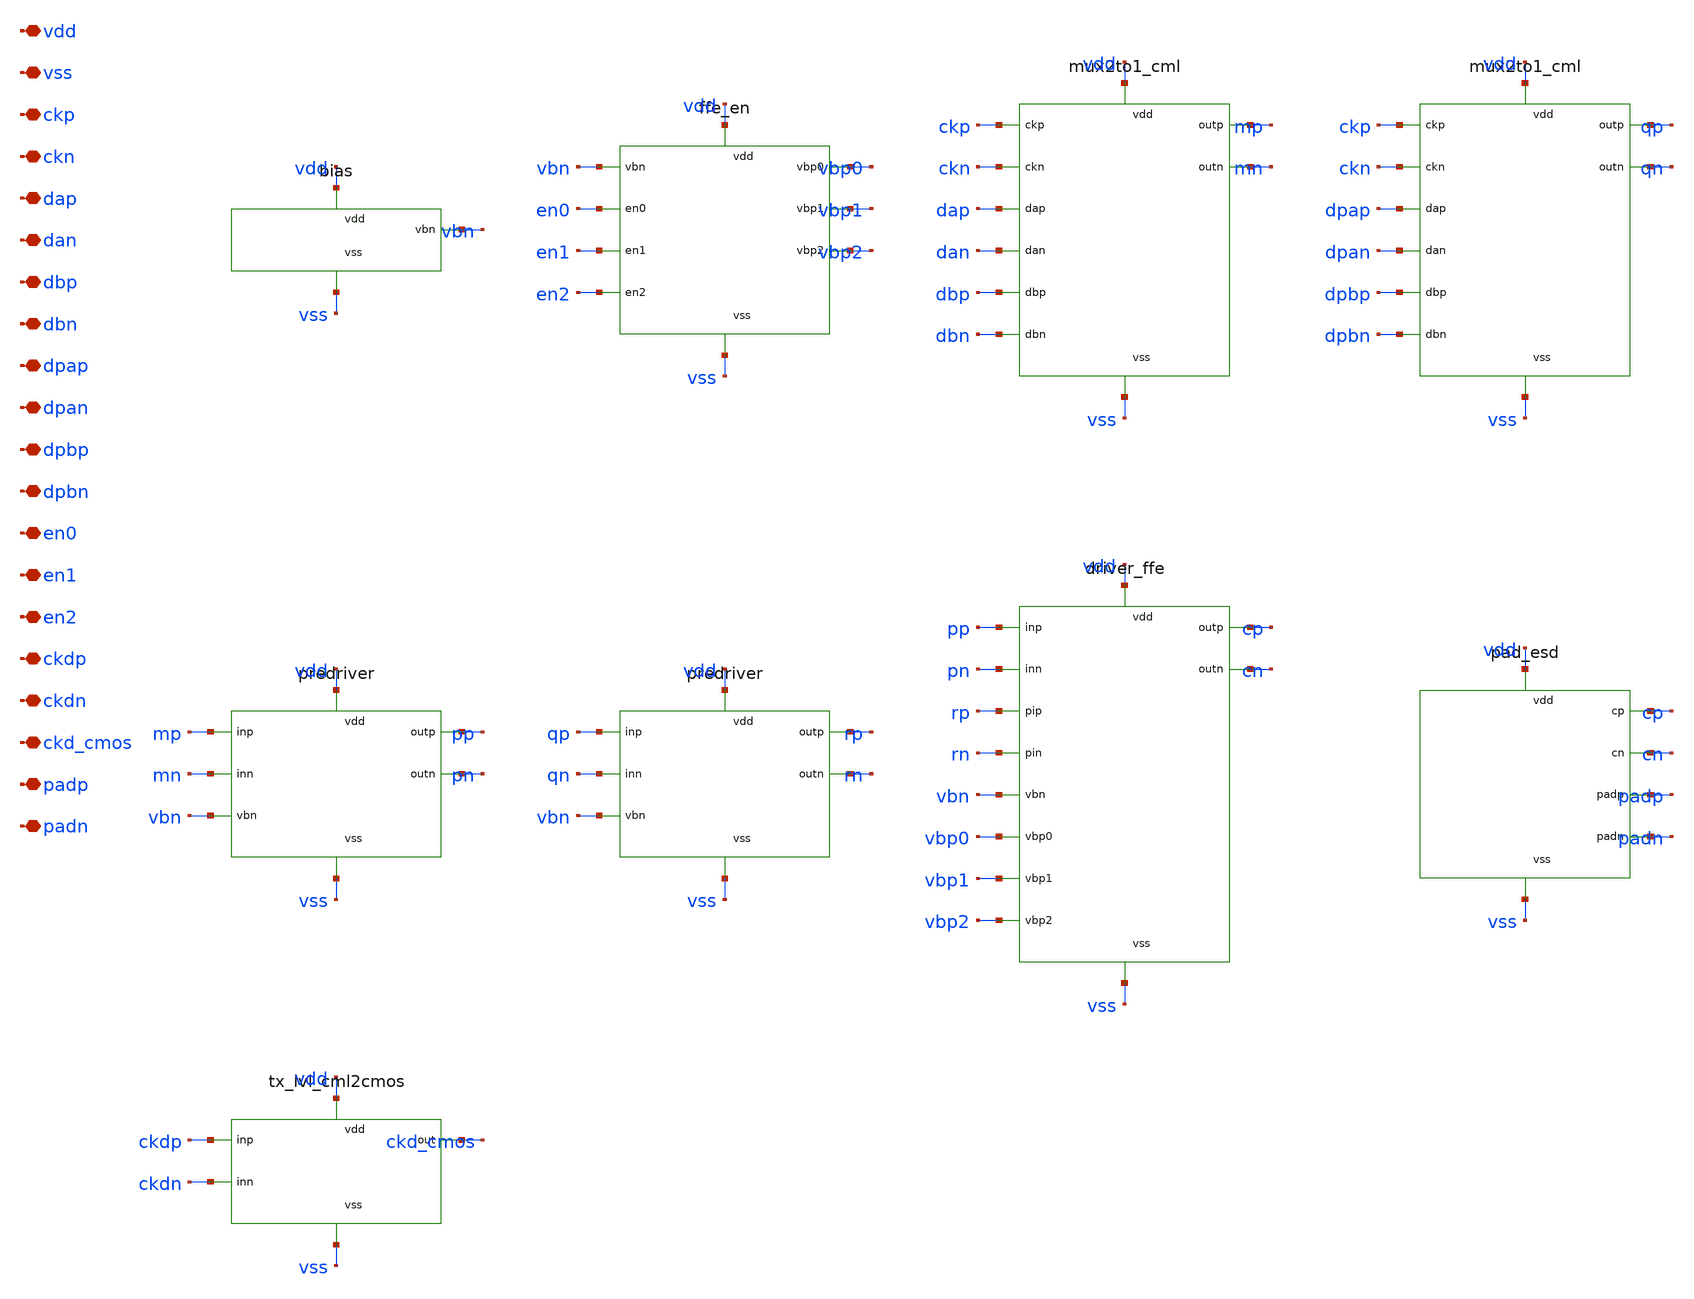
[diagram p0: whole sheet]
** sch_path: design/tx/tx_top.sch
**.subckt tx_top vdd vss ckp ckn dap dan dbp dbn dpap dpan dpbp dpbn en0 en1 en2 ckdp ckdn ckd_cmos
*+ padp padn
*.iopin vdd
*.iopin vss
*.iopin ckp
*.iopin ckn
*.iopin dap
*.iopin dan
*.iopin dbp
*.iopin dbn
*.iopin dpap
*.iopin dpan
*.iopin dpbp
*.iopin dpbn
*.iopin en0
*.iopin en1
*.iopin en2
*.iopin ckdp
*.iopin ckdn
*.iopin ckd_cmos
*.iopin padp
*.iopin padn
Xbias vdd vss vbn bias
Xffe_en vdd vss vbn en0 en1 en2 vbp0 vbp1 vbp2 ffe_en
Xmux_main vdd vss ckp ckn dap dan dbp dbn mp mn mux2to1_cml
Xmux_post vdd vss ckp ckn dpap dpan dpbp dpbn qp qn mux2to1_cml
Xpre_main vdd vss mp mn vbn pp pn predriver
Xpre_post vdd vss qp qn vbn rp rn predriver
Xdrv vdd vss pp pn rp rn vbn vbp0 vbp1 vbp2 cp cn driver_ffe
Xpad vdd vss cp cn padp padn pad_esd
Xlvl vdd vss ckdp ckdn ckd_cmos tx_lvl_cml2cmos
**.ends

* expanding   symbol:  bias.sym # of pins=3
** sym_path: design/tx/bias.sym
** sch_path: design/tx/bias.sch
.subckt bias vdd vss vbn
*.iopin vdd
*.iopin vss
*.iopin vbn
XRref vdd vbn vss rsil w=4u l=114.3u m=1 mm_ok=1
XQref vbn vbn er vss npn13G2 Nx=1 mm_ok=1
XRer er vss vss rsil w=4u l=36.57u m=1 mm_ok=1
XCvbn vbn vss cap_cmim w=7u l=7u m=1 mm_ok=1
.ends


* expanding   symbol:  ffe_en.sym # of pins=9
** sym_path: design/tx/ffe_en.sym
** sch_path: design/tx/ffe_en.sch
.subckt ffe_en vdd vss vbn en0 en1 en2 vbp0 vbp1 vbp2
*.iopin vdd
*.iopin vss
*.iopin vbn
*.iopin en0
*.iopin en1
*.iopin en2
*.iopin vbp0
*.iopin vbp1
*.iopin vbp2
XMPi0 enb0 en0 vdd vdd sg13_lv_pmos w=1u l=0.13u ng=1 m=1 mm_ok=1
XMNi0 enb0 en0 vss vss sg13_lv_nmos w=0.5u l=0.13u ng=1 m=1 mm_ok=1
XRb0 vbn vbp0 vss rsil w=2u l=285.7u m=1 mm_ok=1
XMNd0 vbp0 enb0 vss vss sg13_lv_nmos w=2u l=0.13u ng=1 m=1 mm_ok=1
XMPi1 enb1 en1 vdd vdd sg13_lv_pmos w=1u l=0.13u ng=1 m=1 mm_ok=1
XMNi1 enb1 en1 vss vss sg13_lv_nmos w=0.5u l=0.13u ng=1 m=1 mm_ok=1
XRb1 vbn vbp1 vss rsil w=2u l=285.7u m=1 mm_ok=1
XMNd1 vbp1 enb1 vss vss sg13_lv_nmos w=2u l=0.13u ng=1 m=1 mm_ok=1
XMPi2 enb2 en2 vdd vdd sg13_lv_pmos w=1u l=0.13u ng=1 m=1 mm_ok=1
XMNi2 enb2 en2 vss vss sg13_lv_nmos w=0.5u l=0.13u ng=1 m=1 mm_ok=1
XRb2 vbn vbp2 vss rsil w=2u l=285.7u m=1 mm_ok=1
XMNd2 vbp2 enb2 vss vss sg13_lv_nmos w=2u l=0.13u ng=1 m=1 mm_ok=1
.ends


* expanding   symbol:  mux2to1_cml.sym # of pins=10
** sym_path: design/tx/mux2to1_cml.sym
** sch_path: design/tx/mux2to1_cml.sch
.subckt mux2to1_cml vdd vss ckp ckn dap dan dbp dbn outp outn
*.iopin vdd
*.iopin vss
*.iopin ckp
*.iopin ckn
*.iopin dap
*.iopin dan
*.iopin dbp
*.iopin dbn
*.iopin outp
*.iopin outn
XCca ckp nca cap_cmim w=7u l=7u m=1 mm_ok=1
XRfa mida nca vss rppd w=0.5u l=38.46u m=1 b=0 mm_ok=1
XMP1a mida nca vdd vdd sg13_lv_pmos w=8u l=0.13u ng=2 m=1 mm_ok=1
XMN1a mida nca vss vss sg13_lv_nmos w=4u l=0.13u ng=2 m=1 mm_ok=1
XMP2a sqa mida vdd vdd sg13_lv_pmos w=16u l=0.13u ng=4 m=1 mm_ok=1
XMN2a sqa mida vss vss sg13_lv_nmos w=8u l=0.13u ng=2 m=1 mm_ok=1
XCcb ckn ncb cap_cmim w=7u l=7u m=1 mm_ok=1
XRfb midb ncb vss rppd w=0.5u l=38.46u m=1 b=0 mm_ok=1
XMP1b midb ncb vdd vdd sg13_lv_pmos w=8u l=0.13u ng=2 m=1 mm_ok=1
XMN1b midb ncb vss vss sg13_lv_nmos w=4u l=0.13u ng=2 m=1 mm_ok=1
XMP2b sqb midb vdd vdd sg13_lv_pmos w=16u l=0.13u ng=4 m=1 mm_ok=1
XMN2b sqb midb vss vss sg13_lv_nmos w=8u l=0.13u ng=2 m=1 mm_ok=1
XQa1 outn dap ea vss npn13G2 Nx=2 mm_ok=1
XQa2 outp dan ea vss npn13G2 Nx=2 mm_ok=1
XMTa ea sqa sa vss sg13_lv_nmos w=20u l=0.13u ng=4 m=1 mm_ok=1
XRsa sa vss vss rsil w=8u l=68.57u m=1 mm_ok=1
XQb1 outn dbp eb vss npn13G2 Nx=2 mm_ok=1
XQb2 outp dbn eb vss npn13G2 Nx=2 mm_ok=1
XMTb eb sqb sb vss sg13_lv_nmos w=20u l=0.13u ng=4 m=1 mm_ok=1
XRsb sb vss vss rsil w=8u l=68.57u m=1 mm_ok=1
XRLp vdd outp vss rsil w=8u l=114.3u m=1 mm_ok=1
XRLn vdd outn vss rsil w=8u l=114.3u m=1 mm_ok=1
.ends


* expanding   symbol:  predriver.sym # of pins=7
** sym_path: design/tx/predriver.sym
** sch_path: design/tx/predriver.sch
.subckt predriver vdd vss inp inn vbn outp outn
*.iopin vdd
*.iopin vss
*.iopin inp
*.iopin inn
*.iopin vbn
*.iopin outp
*.iopin outn
XQ1 outn inp e vss npn13G2 Nx=4 mm_ok=1
XQ2 outp inn e vss npn13G2 Nx=4 mm_ok=1
XQt e vbn et vss npn13G2 Nx=4 mm_ok=1
XRe et vss vss rsil w=8u l=18.29u m=1 mm_ok=1
XRL1 vdd outp vss rsil w=8u l=68.57u m=1 mm_ok=1
XRL2 vdd outn vss rsil w=8u l=68.57u m=1 mm_ok=1
.ends


* expanding   symbol:  driver_ffe.sym # of pins=12
** sym_path: design/tx/driver_ffe.sym
** sch_path: design/tx/driver_ffe.sch
.subckt driver_ffe vdd vss inp inn pip pin vbn vbp0 vbp1 vbp2 outp outn
*.iopin vdd
*.iopin vss
*.iopin inp
*.iopin inn
*.iopin pip
*.iopin pin
*.iopin vbn
*.iopin vbp0
*.iopin vbp1
*.iopin vbp2
*.iopin outp
*.iopin outn
XQM1 outn inp em vss npn13G2 Nx=8 mm_ok=1
XQM2 outp inn em vss npn13G2 Nx=8 mm_ok=1
XQTM em vbn etm vss npn13G2 Nx=8 mm_ok=1
XREM etm vss vss rsil w=16u l=18.29u m=1 mm_ok=1
XRT1 vdd outp vss rsil w=16u l=114.3u m=1 mm_ok=1
XRT2 vdd outn vss rsil w=16u l=114.3u m=1 mm_ok=1
XQP0a outp pip ep0 vss npn13G2 Nx=1 mm_ok=1
XQP0b outn pin ep0 vss npn13G2 Nx=1 mm_ok=1
XQTP0 ep0 vbp0 etp0 vss npn13G2 Nx=1 mm_ok=1
XREP0 etp0 vss vss rsil w=4u l=41.14u m=1 mm_ok=1
XQP1a outp pip ep1 vss npn13G2 Nx=1 mm_ok=1
XQP1b outn pin ep1 vss npn13G2 Nx=1 mm_ok=1
XQTP1 ep1 vbp1 etp1 vss npn13G2 Nx=1 mm_ok=1
XREP1 etp1 vss vss rsil w=4u l=41.14u m=1 mm_ok=1
XQP2a outp pip ep2 vss npn13G2 Nx=1 mm_ok=1
XQP2b outn pin ep2 vss npn13G2 Nx=1 mm_ok=1
XQTP2 ep2 vbp2 etp2 vss npn13G2 Nx=1 mm_ok=1
XREP2 etp2 vss vss rsil w=4u l=41.14u m=1 mm_ok=1
.ends


* expanding   symbol:  pad_esd.sym # of pins=6
** sym_path: design/tx/pad_esd.sym
** sch_path: design/tx/pad_esd.sch
.subckt pad_esd vdd vss cp cn padp padn
*.iopin vdd
*.iopin vss
*.iopin cp
*.iopin cn
*.iopin padp
*.iopin padn
XRs0 cp padp vss rsil w=8u l=4.571u m=1 mm_ok=1
XDh0 vdd padp vss diodevdd_2kv m=1
XDl0 vdd padp vss diodevss_2kv m=1
XXPAD0 padp bondpad size=80u shape=0 padtype=0
XRs1 cn padn vss rsil w=8u l=4.571u m=1 mm_ok=1
XDh1 vdd padn vss diodevdd_2kv m=1
XDl1 vdd padn vss diodevss_2kv m=1
XXPAD1 padn bondpad size=80u shape=0 padtype=0
.ends


* expanding   symbol:  tx_lvl_cml2cmos.sym # of pins=5
** sym_path: design/tx/tx_lvl_cml2cmos.sym
** sch_path: design/tx/tx_lvl_cml2cmos.sch
.subckt tx_lvl_cml2cmos vdd vss inp inn out
*.iopin vdd
*.iopin vss
*.iopin inp
*.iopin inn
*.iopin out
XMN1 d1 inp s vss sg13_lv_nmos w=8u l=0.13u ng=2 m=1 mm_ok=1
XMN2 o1 inn s vss sg13_lv_nmos w=8u l=0.13u ng=2 m=1 mm_ok=1
XMP1 d1 d1 vdd vdd sg13_lv_pmos w=8u l=0.13u ng=2 m=1 mm_ok=1
XMP2 o1 d1 vdd vdd sg13_lv_pmos w=8u l=0.13u ng=2 m=1 mm_ok=1
XMNt s vbm vss vss sg13_lv_nmos w=8u l=0.13u ng=2 m=1 mm_ok=1
XMNb vbm vbm vss vss sg13_lv_nmos w=2u l=0.13u ng=1 m=1 mm_ok=1
XRbm vdd vbm vss rppd w=0.5u l=19.23u m=1 b=0 mm_ok=1
XMP3 out o1 vdd vdd sg13_lv_pmos w=4u l=0.13u ng=1 m=1 mm_ok=1
XMN3 out o1 vss vss sg13_lv_nmos w=2u l=0.13u ng=1 m=1 mm_ok=1
.ends

.end
